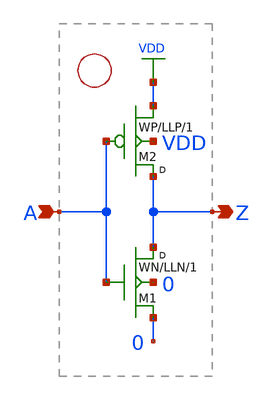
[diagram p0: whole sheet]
** sch_path: xschem_library/examples/cmos_inv.sch
**.subckt cmos_inv Z A
*.opin Z
*.ipin A
M2 Z A VDD VDD p w=WP l=LLP m=1
M1 Z A 0 0 n w=WN l=LLN m=1
**.ends
.GLOBAL VDD
.end
